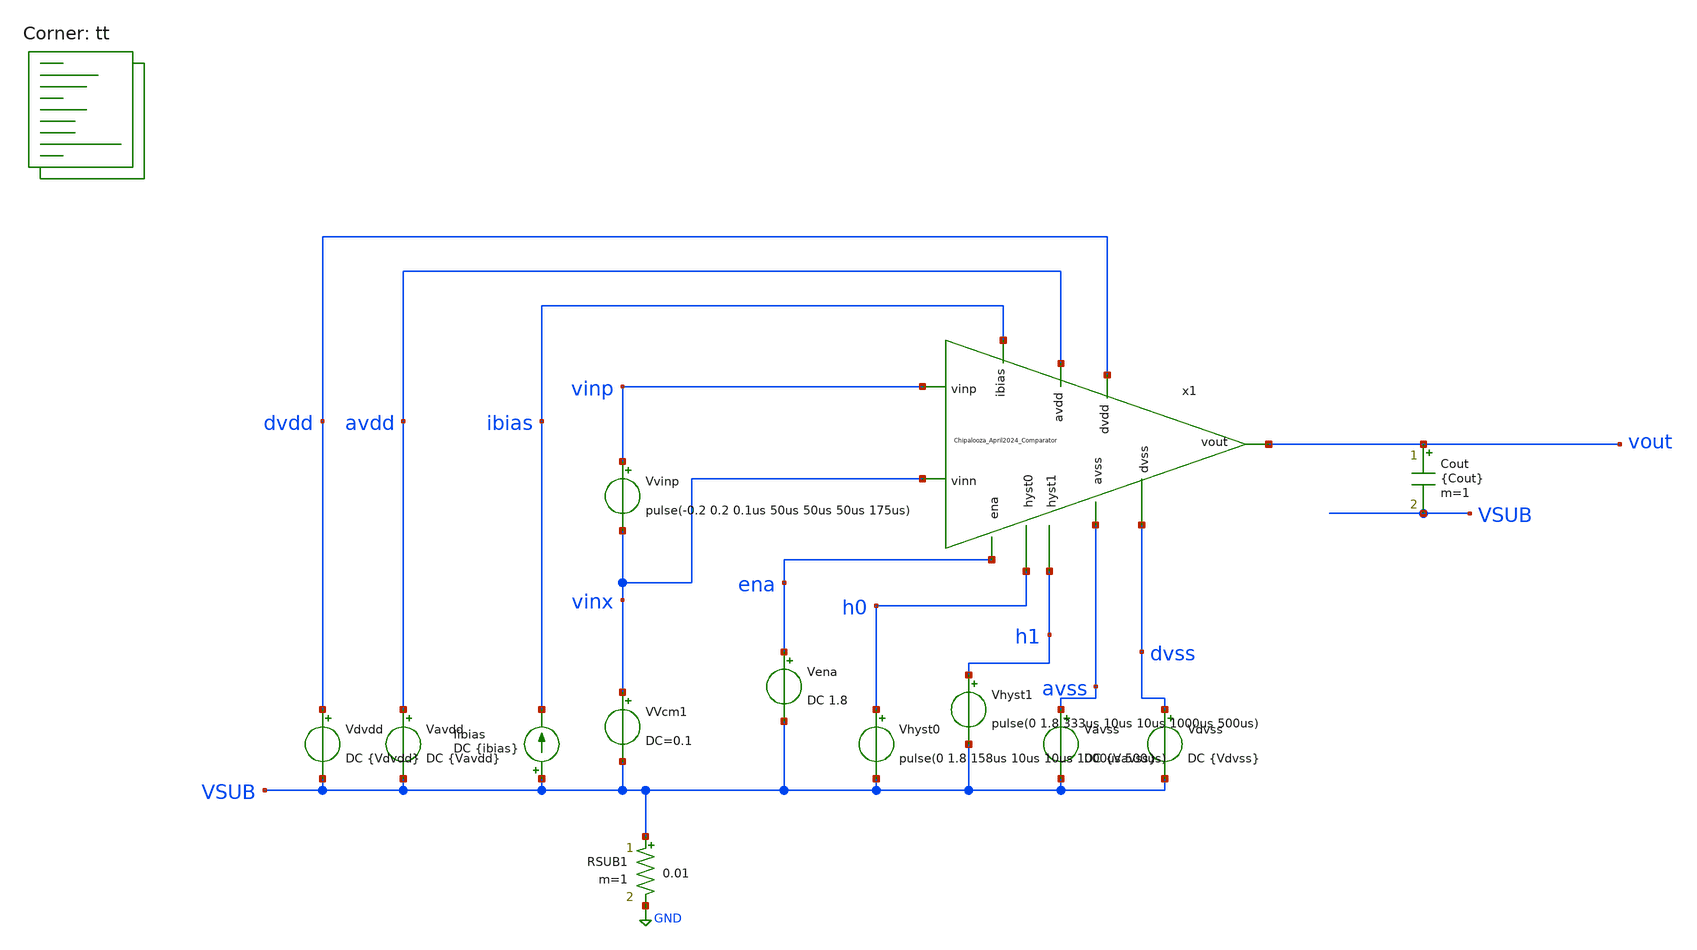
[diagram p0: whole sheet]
** sch_path: Chipalooza_April2024_Comparator/xschem/TB_hysteresis.sch
**.subckt TB_hysteresis
Vavdd avdd VSUB DC {Vavdd}
Vdvdd dvdd VSUB DC {Vdvdd}
Vena ena VSUB DC 1.8
Vhyst0 h0 VSUB pulse(0 1.8 158us 10us 10us 1000us 500us)
Vhyst1 h1 VSUB pulse(0 1.8 333us 10us 10us 1000us 500us)
Vavss avss VSUB DC {Vavss}
Vdvss dvss VSUB DC {Vdvss}
Iibias VSUB ibias DC {ibias}
RSUB1 VSUB GND 0.01 m=1
VVcm1 vinx VSUB DC=0.1
Vvinp vinp vinx pulse(-0.2 0.2 0.1us 50us 50us 50us 175us)
x1 h0 h1 avdd vinp avss vinx dvdd dvss vout ibias ena Chipalooza_April2024_Comparator
Cout vout VSUB {Cout} m=1
**** begin user architecture code

* this option enables mos model bin
* selection based on W/NF instead of W
*.option wnflag=1
.option savecurrents
.option save all
.option temperature=25

.control

.param vavdd=3.3 cout=0 vdvdd=1.8 vavss=0
.param vdvss=0 ibias=2u

*dc VVcm 0 3.3 0.1
*plot v(vout) v(inx)

tran 0.05u 600u
*plot v(vout) v(vinp)

meas tran tr1 TRIG AT=0u TARG v(vout) VAL=1.75 RISE=1
meas tran vin_tr1 find v(vinp) at=tr1

meas tran tf1 TRIG AT=0u TARG v(vout) VAL=0.05 FALL=1
meas tran vin_tf1 find v(vinp) at=tf1

meas tran tr2 TRIG AT=0u TARG v(vout) VAL=1.75 RISE=2
meas tran vin_tr2 find v(vinp) at=tr1

meas tran tf2 TRIG AT=0u TARG v(vout) VAL=0.05 FALL=2
meas tran vin_tf2 find v(vinp) at=tf2

meas tran tr3 TRIG AT=0u TARG v(vout) VAL=1.75 RISE=3
meas tran vin_tr3 find v(vinp) at=tr3

meas tran tf3 TRIG AT=0u TARG v(vout) VAL=0.05 FALL=3
meas tran vin_tf3 find v(vinp) at=tf3

let hyst1=(vin_tf1-vin_tr1)
let hyst2=(vin_tf2-vin_tr2)
let hyst3=(vin_tf3-vin_tr3)

print hyst1
print hyst2
print hyst3

meas tran vinx_tr find v(vinx) at=tr1
let vio=(vinx_tr-vin_tr1)

print vio

write TB_hysteresis.raw

echo $&hyst1 $&hyst2 $&hyst3 $&vio > {simpath}/{filename}_{N}.data


*quit 0

.endc


.lib $::SKYWATER_MODELS/sky130.lib.spice tt
**** end user architecture code
**.ends

* expanding   symbol:  Chipalooza_April2024_Comparator.sym # of pins=11
** sym_path: Chipalooza_April2024_Comparator/xschem/Chipalooza_April2024_Comparator.sym
** sch_path: Chipalooza_April2024_Comparator/xschem/Chipalooza_April2024_Comparator.sch
.subckt Chipalooza_April2024_Comparator hyst0 hyst1 avdd vinp avss vinn dvdd dvss vout ibias ena
*.ipin vinp
*.ipin vinn
*.ipin hyst0
*.ipin hyst1
*.ipin avdd
*.ipin avss
*.ipin dvdd
*.ipin dvss
*.opin vout
*.ipin ena
*.ipin ibias
XM29 SumOutBar SumOut dvdd dvdd sky130_fd_pr__pfet_01v8 L=1 W=2 nf=1 ad='int((nf+1)/2) * W/nf * 0.29'
+ as='int((nf+2)/2) * W/nf * 0.29' pd='2*int((nf+1)/2) * (W/nf + 0.29)' ps='2*int((nf+2)/2) * (W/nf + 0.29)'
+ nrd='0.29 / W' nrs='0.29 / W' sa=0 sb=0 sd=0 mult=2 m=2
XM30 SumOutBar SumOut dvssi dvss sky130_fd_pr__nfet_01v8 L=1 W=2 nf=1 ad='int((nf+1)/2) * W/nf * 0.29'
+ as='int((nf+2)/2) * W/nf * 0.29' pd='2*int((nf+1)/2) * (W/nf + 0.29)' ps='2*int((nf+2)/2) * (W/nf + 0.29)'
+ nrd='0.29 / W' nrs='0.29 / W' sa=0 sb=0 sd=0 mult=2 m=2
XM25 net2 hyst_bias0 avss avss sky130_fd_pr__nfet_g5v0d10v5 L=1 W=3 nf=1 ad='int((nf+1)/2) * W/nf * 0.29'
+ as='int((nf+2)/2) * W/nf * 0.29' pd='2*int((nf+1)/2) * (W/nf + 0.29)' ps='2*int((nf+2)/2) * (W/nf + 0.29)'
+ nrd='0.29 / W' nrs='0.29 / W' sa=0 sb=0 sd=0 mult=2 m=2
XM26 hyst_bias0 ibias dvssi dvss sky130_fd_pr__nfet_01v8 L=1 W=3 nf=1 ad='int((1 + 1)/2) * 3 / 1 * 0.29'
+ as='int((1 + 2)/2) * 3 / 1 * 0.29' pd='2*int((1 + 1)/2) * (3 / 1 + 0.29)' ps='2*int((1 + 2)/2) * (3 / 1 + 0.29)'
+ nrd='0.29 / 3 ' nrs='0.29 / 3 ' sa=0 sb=0 sd=0 mult=2 m=2
XM27 ibias ibias dvssi dvss sky130_fd_pr__nfet_01v8 L=1 W=3 nf=1 ad='int((1 + 1)/2) * 3 / 1 * 0.29' as='int((1 + 2)/2) * 3 / 1 * 0.29'
+ pd='2*int((1 + 1)/2) * (3 / 1 + 0.29)' ps='2*int((1 + 2)/2) * (3 / 1 + 0.29)' nrd='0.29 / 3 ' nrs='0.29 / 3 '
+ sa=0 sb=0 sd=0 mult=2 m=2
XM34 hyst_bias1 hyst_bias0 dvdd dvdd sky130_fd_pr__pfet_01v8 L=1 W=3 nf=1 ad='int((nf+1)/2) * W/nf * 0.29'
+ as='int((nf+2)/2) * W/nf * 0.29' pd='2*int((nf+1)/2) * (W/nf + 0.29)' ps='2*int((nf+2)/2) * (W/nf + 0.29)'
+ nrd='0.29 / W' nrs='0.29 / W' sa=0 sb=0 sd=0 mult=2 m=2
XM35 hyst_bias0 hyst_bias0 dvdd dvdd sky130_fd_pr__pfet_01v8 L=1 W=3 nf=1 ad='int((nf+1)/2) * W/nf * 0.29'
+ as='int((nf+2)/2) * W/nf * 0.29' pd='2*int((nf+1)/2) * (W/nf + 0.29)' ps='2*int((nf+2)/2) * (W/nf + 0.29)'
+ nrd='0.29 / W' nrs='0.29 / W' sa=0 sb=0 sd=0 mult=2 m=2
XM36 dvdd hyst_bias1 dvssi dvss sky130_fd_pr__nfet_01v8 L=1 W=3 nf=1 ad='int((1 + 1)/2) * 3 / 1 * 0.29'
+ as='int((1 + 2)/2) * 3 / 1 * 0.29' pd='2*int((1 + 1)/2) * (3 / 1 + 0.29)' ps='2*int((1 + 2)/2) * (3 / 1 + 0.29)'
+ nrd='0.29 / 3 ' nrs='0.29 / 3 ' sa=0 sb=0 sd=0 mult=2 m=2
XM37 hyst_bias1 hyst_bias1 dvssi dvss sky130_fd_pr__nfet_01v8 L=1 W=3 nf=1 ad='int((1 + 1)/2) * 3 / 1 * 0.29'
+ as='int((1 + 2)/2) * 3 / 1 * 0.29' pd='2*int((1 + 1)/2) * (3 / 1 + 0.29)' ps='2*int((1 + 2)/2) * (3 / 1 + 0.29)'
+ nrd='0.29 / 3 ' nrs='0.29 / 3 ' sa=0 sb=0 sd=0 mult=2 m=2
C1 avss 0 2p m=1
XM38 avssi ena avss avss sky130_fd_pr__nfet_g5v0d10v5 L=1 W=16 nf=1 ad='int((nf+1)/2) * W/nf * 0.29'
+ as='int((nf+2)/2) * W/nf * 0.29' pd='2*int((nf+1)/2) * (W/nf + 0.29)' ps='2*int((nf+2)/2) * (W/nf + 0.29)'
+ nrd='0.29 / W' nrs='0.29 / W' sa=0 sb=0 sd=0 mult=2 m=2
XM39 net3 hyst_bias0 avss avss sky130_fd_pr__nfet_g5v0d10v5 L=1 W=8 nf=1 ad='int((nf+1)/2) * W/nf * 0.29'
+ as='int((nf+2)/2) * W/nf * 0.29' pd='2*int((nf+1)/2) * (W/nf + 0.29)' ps='2*int((nf+2)/2) * (W/nf + 0.29)'
+ nrd='0.29 / W' nrs='0.29 / W' sa=0 sb=0 sd=0 mult=4 m=4
XM40 net1 hyst0 net2 avss sky130_fd_pr__nfet_g5v0d10v5 L=1 W=3 nf=1 ad='int((nf+1)/2) * W/nf * 0.29'
+ as='int((nf+2)/2) * W/nf * 0.29' pd='2*int((nf+1)/2) * (W/nf + 0.29)' ps='2*int((nf+2)/2) * (W/nf + 0.29)'
+ nrd='0.29 / W' nrs='0.29 / W' sa=0 sb=0 sd=0 mult=2 m=2
XM41 net1 hyst1 net3 avss sky130_fd_pr__nfet_g5v0d10v5 L=1 W=8 nf=1 ad='int((nf+1)/2) * W/nf * 0.29'
+ as='int((nf+2)/2) * W/nf * 0.29' pd='2*int((nf+1)/2) * (W/nf + 0.29)' ps='2*int((nf+2)/2) * (W/nf + 0.29)'
+ nrd='0.29 / W' nrs='0.29 / W' sa=0 sb=0 sd=0 mult=4 m=4
C2 avss 0 2p m=1
XM13 dvssi ena avss avss sky130_fd_pr__nfet_g5v0d10v5 L=1 W=16 nf=1 ad='int((nf+1)/2) * W/nf * 0.29'
+ as='int((nf+2)/2) * W/nf * 0.29' pd='2*int((nf+1)/2) * (W/nf + 0.29)' ps='2*int((nf+2)/2) * (W/nf + 0.29)'
+ nrd='0.29 / W' nrs='0.29 / W' sa=0 sb=0 sd=0 mult=2 m=2
XM16 vout SumOutBar dvdd dvdd sky130_fd_pr__pfet_01v8 L=1 W=2 nf=1 ad='int((nf+1)/2) * W/nf * 0.29' as='int((nf+2)/2) * W/nf * 0.29'
+ pd='2*int((nf+1)/2) * (W/nf + 0.29)' ps='2*int((nf+2)/2) * (W/nf + 0.29)' nrd='0.29 / W' nrs='0.29 / W'
+ sa=0 sb=0 sd=0 mult=2 m=2
XM18 vout SumOutBar dvssi dvss sky130_fd_pr__nfet_01v8 L=1 W=2 nf=1 ad='int((nf+1)/2) * W/nf * 0.29'
+ as='int((nf+2)/2) * W/nf * 0.29' pd='2*int((nf+1)/2) * (W/nf + 0.29)' ps='2*int((nf+2)/2) * (W/nf + 0.29)'
+ nrd='0.29 / W' nrs='0.29 / W' sa=0 sb=0 sd=0 mult=2 m=2
XM19 net14 SumOutBar net15 dvdd sky130_fd_pr__pfet_01v8 L=1 W=2 nf=1 ad='int((nf+1)/2) * W/nf * 0.29'
+ as='int((nf+2)/2) * W/nf * 0.29' pd='2*int((nf+1)/2) * (W/nf + 0.29)' ps='2*int((nf+2)/2) * (W/nf + 0.29)'
+ nrd='0.29 / W' nrs='0.29 / W' sa=0 sb=0 sd=0 mult=2 m=2
XM24 net1 SumOut N2 dvdd sky130_fd_pr__pfet_01v8 L=1 W=2 nf=1 ad='int((nf+1)/2) * W/nf * 0.29' as='int((nf+2)/2) * W/nf * 0.29'
+ pd='2*int((nf+1)/2) * (W/nf + 0.29)' ps='2*int((nf+2)/2) * (W/nf + 0.29)' nrd='0.29 / W' nrs='0.29 / W'
+ sa=0 sb=0 sd=0 mult=2 m=2
XM4 SourceBias2 SourceBias2 avdd avdd sky130_fd_pr__pfet_g5v0d10v5 L=1 W=2 nf=1 ad='int((nf+1)/2) * W/nf * 0.29'
+ as='int((nf+2)/2) * W/nf * 0.29' pd='2*int((nf+1)/2) * (W/nf + 0.29)' ps='2*int((nf+2)/2) * (W/nf + 0.29)'
+ nrd='0.29 / W' nrs='0.29 / W' sa=0 sb=0 sd=0 mult=2 m=2
XM5 N1 SourceBias2 avdd avdd sky130_fd_pr__pfet_g5v0d10v5 L=1 W=2 nf=1 ad='int((nf+1)/2) * W/nf * 0.29'
+ as='int((nf+2)/2) * W/nf * 0.29' pd='2*int((nf+1)/2) * (W/nf + 0.29)' ps='2*int((nf+2)/2) * (W/nf + 0.29)'
+ nrd='0.29 / W' nrs='0.29 / W' sa=0 sb=0 sd=0 mult=2 m=2
XM6 N2 SourceBias2 avdd avdd sky130_fd_pr__pfet_g5v0d10v5 L=1 W=2 nf=1 ad='int((nf+1)/2) * W/nf * 0.29'
+ as='int((nf+2)/2) * W/nf * 0.29' pd='2*int((nf+1)/2) * (W/nf + 0.29)' ps='2*int((nf+2)/2) * (W/nf + 0.29)'
+ nrd='0.29 / W' nrs='0.29 / W' sa=0 sb=0 sd=0 mult=2 m=2
XM7 SumOut Bias1 N2 avdd sky130_fd_pr__pfet_g5v0d10v5 L=1 W=2 nf=1 ad='int((nf+1)/2) * W/nf * 0.29' as='int((nf+2)/2) * W/nf * 0.29'
+ pd='2*int((nf+1)/2) * (W/nf + 0.29)' ps='2*int((nf+2)/2) * (W/nf + 0.29)' nrd='0.29 / W' nrs='0.29 / W'
+ sa=0 sb=0 sd=0 mult=2 m=2
XM8 Sum Bias1 N1 avdd sky130_fd_pr__pfet_g5v0d10v5 L=1 W=2 nf=1 ad='int((nf+1)/2) * W/nf * 0.29' as='int((nf+2)/2) * W/nf * 0.29'
+ pd='2*int((nf+1)/2) * (W/nf + 0.29)' ps='2*int((nf+2)/2) * (W/nf + 0.29)' nrd='0.29 / W' nrs='0.29 / W'
+ sa=0 sb=0 sd=0 mult=2 m=2
XM9 SumOut Bias2 P2 avss sky130_fd_pr__nfet_g5v0d10v5 L=1 W=2 nf=1 ad='int((nf+1)/2) * W/nf * 0.29' as='int((nf+2)/2) * W/nf * 0.29'
+ pd='2*int((nf+1)/2) * (W/nf + 0.29)' ps='2*int((nf+2)/2) * (W/nf + 0.29)' nrd='0.29 / W' nrs='0.29 / W'
+ sa=0 sb=0 sd=0 mult=2 m=2
XM10 Sum Bias2 P1 avss sky130_fd_pr__nfet_g5v0d10v5 L=1 W=2 nf=1 ad='int((nf+1)/2) * W/nf * 0.29' as='int((nf+2)/2) * W/nf * 0.29'
+ pd='2*int((nf+1)/2) * (W/nf + 0.29)' ps='2*int((nf+2)/2) * (W/nf + 0.29)' nrd='0.29 / W' nrs='0.29 / W'
+ sa=0 sb=0 sd=0 mult=2 m=2
XM11 P2 Sum avss avss sky130_fd_pr__nfet_g5v0d10v5 L=1 W=2 nf=1 ad='int((nf+1)/2) * W/nf * 0.29' as='int((nf+2)/2) * W/nf * 0.29'
+ pd='2*int((nf+1)/2) * (W/nf + 0.29)' ps='2*int((nf+2)/2) * (W/nf + 0.29)' nrd='0.29 / W' nrs='0.29 / W'
+ sa=0 sb=0 sd=0 mult=2 m=2
XM12 P1 Sum avss avss sky130_fd_pr__nfet_g5v0d10v5 L=1 W=2 nf=1 ad='int((nf+1)/2) * W/nf * 0.29' as='int((nf+2)/2) * W/nf * 0.29'
+ pd='2*int((nf+1)/2) * (W/nf + 0.29)' ps='2*int((nf+2)/2) * (W/nf + 0.29)' nrd='0.29 / W' nrs='0.29 / W'
+ sa=0 sb=0 sd=0 mult=2 m=2
XM2 P2 vinn psource_input avdd sky130_fd_pr__pfet_g5v0d10v5 L=1 W=4 nf=1 ad='int((nf+1)/2) * W/nf * 0.29'
+ as='int((nf+2)/2) * W/nf * 0.29' pd='2*int((nf+1)/2) * (W/nf + 0.29)' ps='2*int((nf+2)/2) * (W/nf + 0.29)'
+ nrd='0.29 / W' nrs='0.29 / W' sa=0 sb=0 sd=0 mult=2 m=2
XM3 P1 vinp psource_input avdd sky130_fd_pr__pfet_g5v0d10v5 L=1 W=4 nf=1 ad='int((nf+1)/2) * W/nf * 0.29'
+ as='int((nf+2)/2) * W/nf * 0.29' pd='2*int((nf+1)/2) * (W/nf + 0.29)' ps='2*int((nf+2)/2) * (W/nf + 0.29)'
+ nrd='0.29 / W' nrs='0.29 / W' sa=0 sb=0 sd=0 mult=2 m=2
XM14 psource_input net4 avdd avdd sky130_fd_pr__pfet_g5v0d10v5 L=1 W=12 nf=1 ad='int((nf+1)/2) * W/nf * 0.29'
+ as='int((nf+2)/2) * W/nf * 0.29' pd='2*int((nf+1)/2) * (W/nf + 0.29)' ps='2*int((nf+2)/2) * (W/nf + 0.29)'
+ nrd='0.29 / W' nrs='0.29 / W' sa=0 sb=0 sd=0 mult=4 m=4
XM15 net4 net4 avdd avdd sky130_fd_pr__pfet_g5v0d10v5 L=1 W=8 nf=1 ad='int((nf+1)/2) * W/nf * 0.29' as='int((nf+2)/2) * W/nf * 0.29'
+ pd='2*int((nf+1)/2) * (W/nf + 0.29)' ps='2*int((nf+2)/2) * (W/nf + 0.29)' nrd='0.29 / W' nrs='0.29 / W'
+ sa=0 sb=0 sd=0 mult=2 m=2
XM17 nbias_tail net6 psource_input avdd sky130_fd_pr__pfet_g5v0d10v5 L=1 W=8 nf=1 ad='int((nf+1)/2) * W/nf * 0.29'
+ as='int((nf+2)/2) * W/nf * 0.29' pd='2*int((nf+1)/2) * (W/nf + 0.29)' ps='2*int((nf+2)/2) * (W/nf + 0.29)'
+ nrd='0.29 / W' nrs='0.29 / W' sa=0 sb=0 sd=0 mult=2 m=2
XM20 N1 vinp SourceBias0 avss sky130_fd_pr__nfet_g5v0d10v5 L=4 W=16 nf=1 ad='int((nf+1)/2) * W/nf * 0.29'
+ as='int((nf+2)/2) * W/nf * 0.29' pd='2*int((nf+1)/2) * (W/nf + 0.29)' ps='2*int((nf+2)/2) * (W/nf + 0.29)'
+ nrd='0.29 / W' nrs='0.29 / W' sa=0 sb=0 sd=0 mult=2 m=2
XM21 N2 vinn SourceBias0 avss sky130_fd_pr__nfet_g5v0d10v5 L=4 W=16 nf=1 ad='int((nf+1)/2) * W/nf * 0.29'
+ as='int((nf+2)/2) * W/nf * 0.29' pd='2*int((nf+1)/2) * (W/nf + 0.29)' ps='2*int((nf+2)/2) * (W/nf + 0.29)'
+ nrd='0.29 / W' nrs='0.29 / W' sa=0 sb=0 sd=0 mult=2 m=2
XM22 SourceBias0 nbias_tail avssi avss sky130_fd_pr__nfet_g5v0d10v5 L=1 W=12 nf=1 ad='int((nf+1)/2) * W/nf * 0.29'
+ as='int((nf+2)/2) * W/nf * 0.29' pd='2*int((nf+1)/2) * (W/nf + 0.29)' ps='2*int((nf+2)/2) * (W/nf + 0.29)'
+ nrd='0.29 / W' nrs='0.29 / W' sa=0 sb=0 sd=0 mult=4 m=4
XM23 nbias_tail nbias_tail avssi avss sky130_fd_pr__nfet_g5v0d10v5 L=1 W=12 nf=1 ad='int((nf+1)/2) * W/nf * 0.29'
+ as='int((nf+2)/2) * W/nf * 0.29' pd='2*int((nf+1)/2) * (W/nf + 0.29)' ps='2*int((nf+2)/2) * (W/nf + 0.29)'
+ nrd='0.29 / W' nrs='0.29 / W' sa=0 sb=0 sd=0 mult=2 m=2
XM28 net4 Bias5 SourceBias0 avss sky130_fd_pr__nfet_g5v0d10v5 L=1 W=4 nf=1 ad='int((nf+1)/2) * W/nf * 0.29'
+ as='int((nf+2)/2) * W/nf * 0.29' pd='2*int((nf+1)/2) * (W/nf + 0.29)' ps='2*int((nf+2)/2) * (W/nf + 0.29)'
+ nrd='0.29 / W' nrs='0.29 / W' sa=0 sb=0 sd=0 mult=2 m=2
XM31 SourceBias0 net5 avssi avss sky130_fd_pr__nfet_g5v0d10v5 L=4 W=16 nf=1 ad='int((nf+1)/2) * W/nf * 0.29'
+ as='int((nf+2)/2) * W/nf * 0.29' pd='2*int((nf+1)/2) * (W/nf + 0.29)' ps='2*int((nf+2)/2) * (W/nf + 0.29)'
+ nrd='0.29 / W' nrs='0.29 / W' sa=0 sb=0 sd=0 mult=2 m=2
XM44 net5 net5 avssi avss sky130_fd_pr__nfet_g5v0d10v5 L=4 W=16 nf=1 ad='int((nf+1)/2) * W/nf * 0.29'
+ as='int((nf+2)/2) * W/nf * 0.29' pd='2*int((nf+1)/2) * (W/nf + 0.29)' ps='2*int((nf+2)/2) * (W/nf + 0.29)'
+ nrd='0.29 / W' nrs='0.29 / W' sa=0 sb=0 sd=0 mult=2 m=2
XM45 SourceBias1 net5 avssi avss sky130_fd_pr__nfet_g5v0d10v5 L=4 W=16 nf=1 ad='int((nf+1)/2) * W/nf * 0.29'
+ as='int((nf+2)/2) * W/nf * 0.29' pd='2*int((nf+1)/2) * (W/nf + 0.29)' ps='2*int((nf+2)/2) * (W/nf + 0.29)'
+ nrd='0.29 / W' nrs='0.29 / W' sa=0 sb=0 sd=0 mult=2 m=2
XM46 SourceBias1 SourceBias1 avdd avdd sky130_fd_pr__pfet_g5v0d10v5 L=1 W=12 nf=1 ad='int((nf+1)/2) * W/nf * 0.29'
+ as='int((nf+2)/2) * W/nf * 0.29' pd='2*int((nf+1)/2) * (W/nf + 0.29)' ps='2*int((nf+2)/2) * (W/nf + 0.29)'
+ nrd='0.29 / W' nrs='0.29 / W' sa=0 sb=0 sd=0 mult=4 m=4
XM47 psource_input SourceBias1 avdd avdd sky130_fd_pr__pfet_g5v0d10v5 L=1 W=12 nf=1 ad='int((nf+1)/2) * W/nf * 0.29'
+ as='int((nf+2)/2) * W/nf * 0.29' pd='2*int((nf+1)/2) * (W/nf + 0.29)' ps='2*int((nf+2)/2) * (W/nf + 0.29)'
+ nrd='0.29 / W' nrs='0.29 / W' sa=0 sb=0 sd=0 mult=4 m=4
XM48 SourceBias2 net5 avssi avss sky130_fd_pr__nfet_g5v0d10v5 L=4 W=16 nf=1 ad='int((nf+1)/2) * W/nf * 0.29'
+ as='int((nf+2)/2) * W/nf * 0.29' pd='2*int((nf+1)/2) * (W/nf + 0.29)' ps='2*int((nf+2)/2) * (W/nf + 0.29)'
+ nrd='0.29 / W' nrs='0.29 / W' sa=0 sb=0 sd=0 mult=4 m=4
XM63 net6 net6 avdd avdd sky130_fd_pr__pfet_g5v0d10v5 L=5 W=3 nf=1 ad='int((nf+1)/2) * W/nf * 0.29' as='int((nf+2)/2) * W/nf * 0.29'
+ pd='2*int((nf+1)/2) * (W/nf + 0.29)' ps='2*int((nf+2)/2) * (W/nf + 0.29)' nrd='0.29 / W' nrs='0.29 / W'
+ sa=0 sb=0 sd=0 mult=1 m=1
XM62 avdd Bias4 SourceBias3 avss sky130_fd_pr__nfet_g5v0d10v5 L=1 W=4 nf=1 ad='int((nf+1)/2) * W/nf * 0.29'
+ as='int((nf+2)/2) * W/nf * 0.29' pd='2*int((nf+1)/2) * (W/nf + 0.29)' ps='2*int((nf+2)/2) * (W/nf + 0.29)'
+ nrd='0.29 / W' nrs='0.29 / W' sa=0 sb=0 sd=0 mult=2 m=2
XM64 net6 Bias4 SourceBias3 avss sky130_fd_pr__nfet_g5v0d10v5 L=1 W=4 nf=1 ad='int((nf+1)/2) * W/nf * 0.29'
+ as='int((nf+2)/2) * W/nf * 0.29' pd='2*int((nf+1)/2) * (W/nf + 0.29)' ps='2*int((nf+2)/2) * (W/nf + 0.29)'
+ nrd='0.29 / W' nrs='0.29 / W' sa=0 sb=0 sd=0 mult=2 m=2
XM65 SourceBias3 net5 avssi avss sky130_fd_pr__nfet_g5v0d10v5 L=4 W=16 nf=1 ad='int((nf+1)/2) * W/nf * 0.29'
+ as='int((nf+2)/2) * W/nf * 0.29' pd='2*int((nf+1)/2) * (W/nf + 0.29)' ps='2*int((nf+2)/2) * (W/nf + 0.29)'
+ nrd='0.29 / W' nrs='0.29 / W' sa=0 sb=0 sd=0 mult=4 m=4
XM76 Bias1 net5 avssi avss sky130_fd_pr__nfet_g5v0d10v5 L=4 W=16 nf=1 ad='int((nf+1)/2) * W/nf * 0.29'
+ as='int((nf+2)/2) * W/nf * 0.29' pd='2*int((nf+1)/2) * (W/nf + 0.29)' ps='2*int((nf+2)/2) * (W/nf + 0.29)'
+ nrd='0.29 / W' nrs='0.29 / W' sa=0 sb=0 sd=0 mult=4 m=4
XM77 SourceBias5 net5 avssi avss sky130_fd_pr__nfet_g5v0d10v5 L=4 W=16 nf=1 ad='int((nf+1)/2) * W/nf * 0.29'
+ as='int((nf+2)/2) * W/nf * 0.29' pd='2*int((nf+1)/2) * (W/nf + 0.29)' ps='2*int((nf+2)/2) * (W/nf + 0.29)'
+ nrd='0.29 / W' nrs='0.29 / W' sa=0 sb=0 sd=0 mult=4 m=4
XM78 SourceBias6 net5 avssi avss sky130_fd_pr__nfet_g5v0d10v5 L=4 W=16 nf=1 ad='int((nf+1)/2) * W/nf * 0.29'
+ as='int((nf+2)/2) * W/nf * 0.29' pd='2*int((nf+1)/2) * (W/nf + 0.29)' ps='2*int((nf+2)/2) * (W/nf + 0.29)'
+ nrd='0.29 / W' nrs='0.29 / W' sa=0 sb=0 sd=0 mult=4 m=4
XM79 SourceBias7 net5 avssi avss sky130_fd_pr__nfet_g5v0d10v5 L=4 W=16 nf=1 ad='int((nf+1)/2) * W/nf * 0.29'
+ as='int((nf+2)/2) * W/nf * 0.29' pd='2*int((nf+1)/2) * (W/nf + 0.29)' ps='2*int((nf+2)/2) * (W/nf + 0.29)'
+ nrd='0.29 / W' nrs='0.29 / W' sa=0 sb=0 sd=0 mult=4 m=4
XM81 Bias5 net5 avssi avss sky130_fd_pr__nfet_g5v0d10v5 L=4 W=16 nf=1 ad='int((nf+1)/2) * W/nf * 0.29'
+ as='int((nf+2)/2) * W/nf * 0.29' pd='2*int((nf+1)/2) * (W/nf + 0.29)' ps='2*int((nf+2)/2) * (W/nf + 0.29)'
+ nrd='0.29 / W' nrs='0.29 / W' sa=0 sb=0 sd=0 mult=4 m=4
XM82 Bias4 net5 avssi avss sky130_fd_pr__nfet_g5v0d10v5 L=4 W=16 nf=1 ad='int((nf+1)/2) * W/nf * 0.29'
+ as='int((nf+2)/2) * W/nf * 0.29' pd='2*int((nf+1)/2) * (W/nf + 0.29)' ps='2*int((nf+2)/2) * (W/nf + 0.29)'
+ nrd='0.29 / W' nrs='0.29 / W' sa=0 sb=0 sd=0 mult=4 m=4
XM83 SourceBias10 net5 avssi avss sky130_fd_pr__nfet_g5v0d10v5 L=4 W=16 nf=1 ad='int((nf+1)/2) * W/nf * 0.29'
+ as='int((nf+2)/2) * W/nf * 0.29' pd='2*int((nf+1)/2) * (W/nf + 0.29)' ps='2*int((nf+2)/2) * (W/nf + 0.29)'
+ nrd='0.29 / W' nrs='0.29 / W' sa=0 sb=0 sd=0 mult=4 m=4
XM1 ibias ibias avssi avss sky130_fd_pr__nfet_g5v0d10v5 L=4 W=16 nf=1 ad='int((nf+1)/2) * W/nf * 0.29'
+ as='int((nf+2)/2) * W/nf * 0.29' pd='2*int((nf+1)/2) * (W/nf + 0.29)' ps='2*int((nf+2)/2) * (W/nf + 0.29)'
+ nrd='0.29 / W' nrs='0.29 / W' sa=0 sb=0 sd=0 mult=2 m=2
XM32 net7 ibias avssi avss sky130_fd_pr__nfet_g5v0d10v5 L=4 W=16 nf=1 ad='int((nf+1)/2) * W/nf * 0.29'
+ as='int((nf+2)/2) * W/nf * 0.29' pd='2*int((nf+1)/2) * (W/nf + 0.29)' ps='2*int((nf+2)/2) * (W/nf + 0.29)'
+ nrd='0.29 / W' nrs='0.29 / W' sa=0 sb=0 sd=0 mult=2 m=2
XM33 net7 net7 avdd avdd sky130_fd_pr__pfet_g5v0d10v5 L=1 W=8 nf=1 ad='int((nf+1)/2) * W/nf * 0.29' as='int((nf+2)/2) * W/nf * 0.29'
+ pd='2*int((nf+1)/2) * (W/nf + 0.29)' ps='2*int((nf+2)/2) * (W/nf + 0.29)' nrd='0.29 / W' nrs='0.29 / W'
+ sa=0 sb=0 sd=0 mult=2 m=2
XM42 net5 net7 avdd avdd sky130_fd_pr__pfet_g5v0d10v5 L=1 W=8 nf=1 ad='int((nf+1)/2) * W/nf * 0.29' as='int((nf+2)/2) * W/nf * 0.29'
+ pd='2*int((nf+1)/2) * (W/nf + 0.29)' ps='2*int((nf+2)/2) * (W/nf + 0.29)' nrd='0.29 / W' nrs='0.29 / W'
+ sa=0 sb=0 sd=0 mult=2 m=2
XM54 M55Source M55Drain avss avss sky130_fd_pr__nfet_g5v0d10v5 L=1.5 W=6 nf=1 ad='int((nf+1)/2) * W/nf * 0.29'
+ as='int((nf+2)/2) * W/nf * 0.29' pd='2*int((nf+1)/2) * (W/nf + 0.29)' ps='2*int((nf+2)/2) * (W/nf + 0.29)'
+ nrd='0.29 / W' nrs='0.29 / W' sa=0 sb=0 sd=0 mult=2 m=2
XM55 M55Drain Bias2 M55Source avss sky130_fd_pr__nfet_g5v0d10v5 L=1 W=9 nf=1 ad='int((nf+1)/2) * W/nf * 0.29'
+ as='int((nf+2)/2) * W/nf * 0.29' pd='2*int((nf+1)/2) * (W/nf + 0.29)' ps='2*int((nf+2)/2) * (W/nf + 0.29)'
+ nrd='0.29 / W' nrs='0.29 / W' sa=0 sb=0 sd=0 mult=2 m=2
XM56 Bias2 Bias2 avss avss sky130_fd_pr__nfet_g5v0d10v5 L=2 W=0.5 nf=1 ad='int((nf+1)/2) * W/nf * 0.29'
+ as='int((nf+2)/2) * W/nf * 0.29' pd='2*int((nf+1)/2) * (W/nf + 0.29)' ps='2*int((nf+2)/2) * (W/nf + 0.29)'
+ nrd='0.29 / W' nrs='0.29 / W' sa=0 sb=0 sd=0 mult=1 m=1
XM51 net8 net9 avdd avdd sky130_fd_pr__pfet_g5v0d10v5 L=2 W=20 nf=1 ad='int((nf+1)/2) * W/nf * 0.29'
+ as='int((nf+2)/2) * W/nf * 0.29' pd='2*int((nf+1)/2) * (W/nf + 0.29)' ps='2*int((nf+2)/2) * (W/nf + 0.29)'
+ nrd='0.29 / W' nrs='0.29 / W' sa=0 sb=0 sd=0 mult=2 m=2
XM49 net9 net9 avdd avdd sky130_fd_pr__pfet_g5v0d10v5 L=2 W=10 nf=1 ad='int((nf+1)/2) * W/nf * 0.29'
+ as='int((nf+2)/2) * W/nf * 0.29' pd='2*int((nf+1)/2) * (W/nf + 0.29)' ps='2*int((nf+2)/2) * (W/nf + 0.29)'
+ nrd='0.29 / W' nrs='0.29 / W' sa=0 sb=0 sd=0 mult=2 m=2
XM50 SourceBias4 SourceBias4 net9 avdd sky130_fd_pr__pfet_g5v0d10v5 L=1 W=10 nf=1 ad='int((nf+1)/2) * W/nf * 0.29'
+ as='int((nf+2)/2) * W/nf * 0.29' pd='2*int((nf+1)/2) * (W/nf + 0.29)' ps='2*int((nf+2)/2) * (W/nf + 0.29)'
+ nrd='0.29 / W' nrs='0.29 / W' sa=0 sb=0 sd=0 mult=2 m=2
XM52 avss SourceBias4 net8 avdd sky130_fd_pr__pfet_g5v0d10v5 L=1 W=1 nf=1 ad='int((nf+1)/2) * W/nf * 0.29'
+ as='int((nf+2)/2) * W/nf * 0.29' pd='2*int((nf+1)/2) * (W/nf + 0.29)' ps='2*int((nf+2)/2) * (W/nf + 0.29)'
+ nrd='0.29 / W' nrs='0.29 / W' sa=0 sb=0 sd=0 mult=2 m=2
XM53 Bias1 Bias1 net8 avdd sky130_fd_pr__pfet_g5v0d10v5 L=1 W=10 nf=1 ad='int((nf+1)/2) * W/nf * 0.29'
+ as='int((nf+2)/2) * W/nf * 0.29' pd='2*int((nf+1)/2) * (W/nf + 0.29)' ps='2*int((nf+2)/2) * (W/nf + 0.29)'
+ nrd='0.29 / W' nrs='0.29 / W' sa=0 sb=0 sd=0 mult=2 m=2
XM57 net10 net11 avdd avdd sky130_fd_pr__pfet_g5v0d10v5 L=2 W=20 nf=1 ad='int((nf+1)/2) * W/nf * 0.29'
+ as='int((nf+2)/2) * W/nf * 0.29' pd='2*int((nf+1)/2) * (W/nf + 0.29)' ps='2*int((nf+2)/2) * (W/nf + 0.29)'
+ nrd='0.29 / W' nrs='0.29 / W' sa=0 sb=0 sd=0 mult=2 m=2
XM58 net11 net11 avdd avdd sky130_fd_pr__pfet_g5v0d10v5 L=2 W=10 nf=1 ad='int((nf+1)/2) * W/nf * 0.29'
+ as='int((nf+2)/2) * W/nf * 0.29' pd='2*int((nf+1)/2) * (W/nf + 0.29)' ps='2*int((nf+2)/2) * (W/nf + 0.29)'
+ nrd='0.29 / W' nrs='0.29 / W' sa=0 sb=0 sd=0 mult=2 m=2
XM59 SourceBias10 SourceBias10 net11 avdd sky130_fd_pr__pfet_g5v0d10v5 L=1 W=10 nf=1 ad='int((nf+1)/2) * W/nf * 0.29'
+ as='int((nf+2)/2) * W/nf * 0.29' pd='2*int((nf+1)/2) * (W/nf + 0.29)' ps='2*int((nf+2)/2) * (W/nf + 0.29)'
+ nrd='0.29 / W' nrs='0.29 / W' sa=0 sb=0 sd=0 mult=2 m=2
XM60 avss SourceBias10 net10 avdd sky130_fd_pr__pfet_g5v0d10v5 L=1 W=1 nf=1 ad='int((nf+1)/2) * W/nf * 0.29'
+ as='int((nf+2)/2) * W/nf * 0.29' pd='2*int((nf+1)/2) * (W/nf + 0.29)' ps='2*int((nf+2)/2) * (W/nf + 0.29)'
+ nrd='0.29 / W' nrs='0.29 / W' sa=0 sb=0 sd=0 mult=2 m=2
XM61 Bias4 Bias4 net10 avdd sky130_fd_pr__pfet_g5v0d10v5 L=1 W=5 nf=1 ad='int((nf+1)/2) * W/nf * 0.29'
+ as='int((nf+2)/2) * W/nf * 0.29' pd='2*int((nf+1)/2) * (W/nf + 0.29)' ps='2*int((nf+2)/2) * (W/nf + 0.29)'
+ nrd='0.29 / W' nrs='0.29 / W' sa=0 sb=0 sd=0 mult=2 m=2
XM66 net12 net13 avdd avdd sky130_fd_pr__pfet_g5v0d10v5 L=2 W=20 nf=1 ad='int((nf+1)/2) * W/nf * 0.29'
+ as='int((nf+2)/2) * W/nf * 0.29' pd='2*int((nf+1)/2) * (W/nf + 0.29)' ps='2*int((nf+2)/2) * (W/nf + 0.29)'
+ nrd='0.29 / W' nrs='0.29 / W' sa=0 sb=0 sd=0 mult=2 m=2
XM67 net13 net13 avdd avdd sky130_fd_pr__pfet_g5v0d10v5 L=2 W=20 nf=1 ad='int((nf+1)/2) * W/nf * 0.29'
+ as='int((nf+2)/2) * W/nf * 0.29' pd='2*int((nf+1)/2) * (W/nf + 0.29)' ps='2*int((nf+2)/2) * (W/nf + 0.29)'
+ nrd='0.29 / W' nrs='0.29 / W' sa=0 sb=0 sd=0 mult=2 m=2
XM68 SourceBias7 SourceBias7 net13 avdd sky130_fd_pr__pfet_g5v0d10v5 L=1 W=10 nf=1 ad='int((nf+1)/2) * W/nf * 0.29'
+ as='int((nf+2)/2) * W/nf * 0.29' pd='2*int((nf+1)/2) * (W/nf + 0.29)' ps='2*int((nf+2)/2) * (W/nf + 0.29)'
+ nrd='0.29 / W' nrs='0.29 / W' sa=0 sb=0 sd=0 mult=2 m=2
XM69 avss SourceBias7 net12 avdd sky130_fd_pr__pfet_g5v0d10v5 L=1 W=1 nf=1 ad='int((nf+1)/2) * W/nf * 0.29'
+ as='int((nf+2)/2) * W/nf * 0.29' pd='2*int((nf+1)/2) * (W/nf + 0.29)' ps='2*int((nf+2)/2) * (W/nf + 0.29)'
+ nrd='0.29 / W' nrs='0.29 / W' sa=0 sb=0 sd=0 mult=2 m=2
XM70 Bias5 Bias5 net12 avdd sky130_fd_pr__pfet_g5v0d10v5 L=1 W=5 nf=1 ad='int((nf+1)/2) * W/nf * 0.29'
+ as='int((nf+2)/2) * W/nf * 0.29' pd='2*int((nf+1)/2) * (W/nf + 0.29)' ps='2*int((nf+2)/2) * (W/nf + 0.29)'
+ nrd='0.29 / W' nrs='0.29 / W' sa=0 sb=0 sd=0 mult=2 m=2
XM72 SourceBias5 SourceBias5 avdd avdd sky130_fd_pr__pfet_g5v0d10v5 L=1 W=12 nf=1 ad='int((nf+1)/2) * W/nf * 0.29'
+ as='int((nf+2)/2) * W/nf * 0.29' pd='2*int((nf+1)/2) * (W/nf + 0.29)' ps='2*int((nf+2)/2) * (W/nf + 0.29)'
+ nrd='0.29 / W' nrs='0.29 / W' sa=0 sb=0 sd=0 mult=4 m=4
XM73 M55Drain SourceBias5 avdd avdd sky130_fd_pr__pfet_g5v0d10v5 L=1 W=12 nf=1 ad='int((nf+1)/2) * W/nf * 0.29'
+ as='int((nf+2)/2) * W/nf * 0.29' pd='2*int((nf+1)/2) * (W/nf + 0.29)' ps='2*int((nf+2)/2) * (W/nf + 0.29)'
+ nrd='0.29 / W' nrs='0.29 / W' sa=0 sb=0 sd=0 mult=4 m=4
XM74 SourceBias6 SourceBias6 avdd avdd sky130_fd_pr__pfet_g5v0d10v5 L=1 W=12 nf=1 ad='int((nf+1)/2) * W/nf * 0.29'
+ as='int((nf+2)/2) * W/nf * 0.29' pd='2*int((nf+1)/2) * (W/nf + 0.29)' ps='2*int((nf+2)/2) * (W/nf + 0.29)'
+ nrd='0.29 / W' nrs='0.29 / W' sa=0 sb=0 sd=0 mult=4 m=4
XM75 Bias2 SourceBias6 avdd avdd sky130_fd_pr__pfet_g5v0d10v5 L=1 W=12 nf=1 ad='int((nf+1)/2) * W/nf * 0.29'
+ as='int((nf+2)/2) * W/nf * 0.29' pd='2*int((nf+1)/2) * (W/nf + 0.29)' ps='2*int((nf+2)/2) * (W/nf + 0.29)'
+ nrd='0.29 / W' nrs='0.29 / W' sa=0 sb=0 sd=0 mult=4 m=4
.ends

.GLOBAL GND
.end
